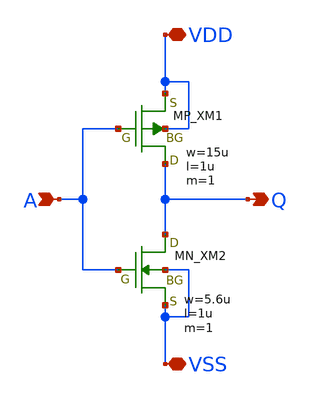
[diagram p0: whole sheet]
** sch_path: schematic/20250924_OSS_Workshop/Qdai/inverter_MUX_02/inv_niimi.sch
**.subckt inv_niimi VDD VSS Q A
*.iopin VDD
*.iopin VSS
*.opin Q
*.ipin A
XM1 Q A VDD VDD PMOS w=15u l=1u as=0 ad=0 ps=0 pd=0 nrd=0 nrs=0 m=1
XM2 Q A VSS VSS NMOS w=5.6u l=1u as=0 ad=0 ps=0 pd=0 nrd=0 nrs=0 m=1
**.ends
.end
